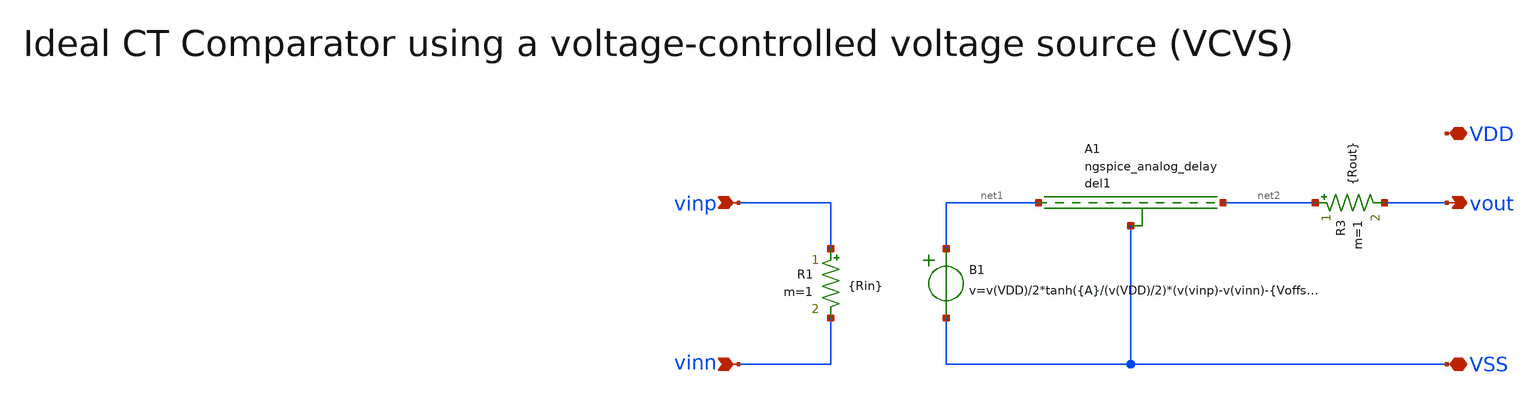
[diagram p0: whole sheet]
** sch_path: SG13G2_ATBS-ADC-main/xschem/comparator/continuous_time/ideal/CT_comparator_ideal.sch
**.subckt CT_comparator_ideal vinn vout vinp VSS VDD
*.ipin vinn
*.opin vout
*.ipin vinp
*.iopin VSS
*.iopin VDD
R1 vinp vinn {Rin} m=1
B1 net1 VSS v=v(VDD)/2*tanh({A}/(v(VDD)/2)*(v(vinp)-v(vinn)-{Voffs}))+{Vcm}
R3 net2 vout {Rout} m=1
A1 net1 net2 VSS del_subckt
.model del_subckt delay(delay=tpd buffer_size=8192)
**.ends
.end
